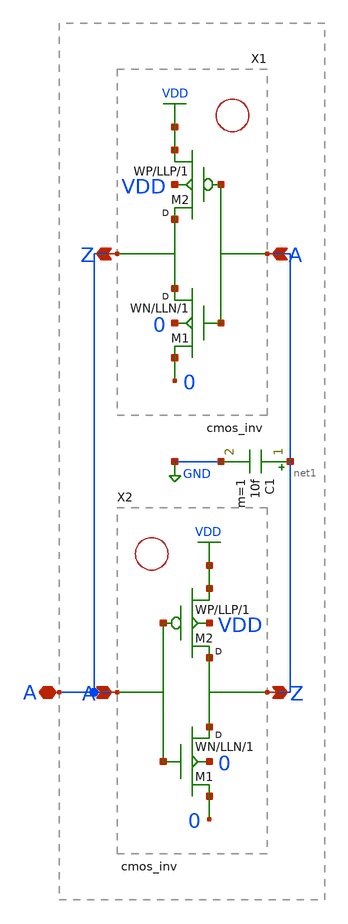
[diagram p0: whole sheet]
** sch_path: xschem_library/examples/bus_keeper.sch
**.subckt bus_keeper A
*.iopin A
X2 net1 A cmos_inv WN=15u WP=45u LLN=3u LLP=3u m=1
X1 A net1 cmos_inv WN=WN_FB WP=WP_FB LLN=3u LLP=3u m=1
C1 net1 GND 10f m=1
**.ends

* expanding   symbol:  cmos_inv.sch # of pins=2
** sym_path: xschem_library/examples/cmos_inv.sch
** sch_path: xschem_library/examples/cmos_inv.sch
.subckt cmos_inv Z A  WN=15u WP=45u LLN=3u LLP=3u
*.ipin A
*.opin Z
M1 Z A 0 0 n w=WN l=LLN m=1
M2 Z A VDD VDD p w=WP l=LLP m=1
.ends

.GLOBAL GND
.GLOBAL VDD
.end
